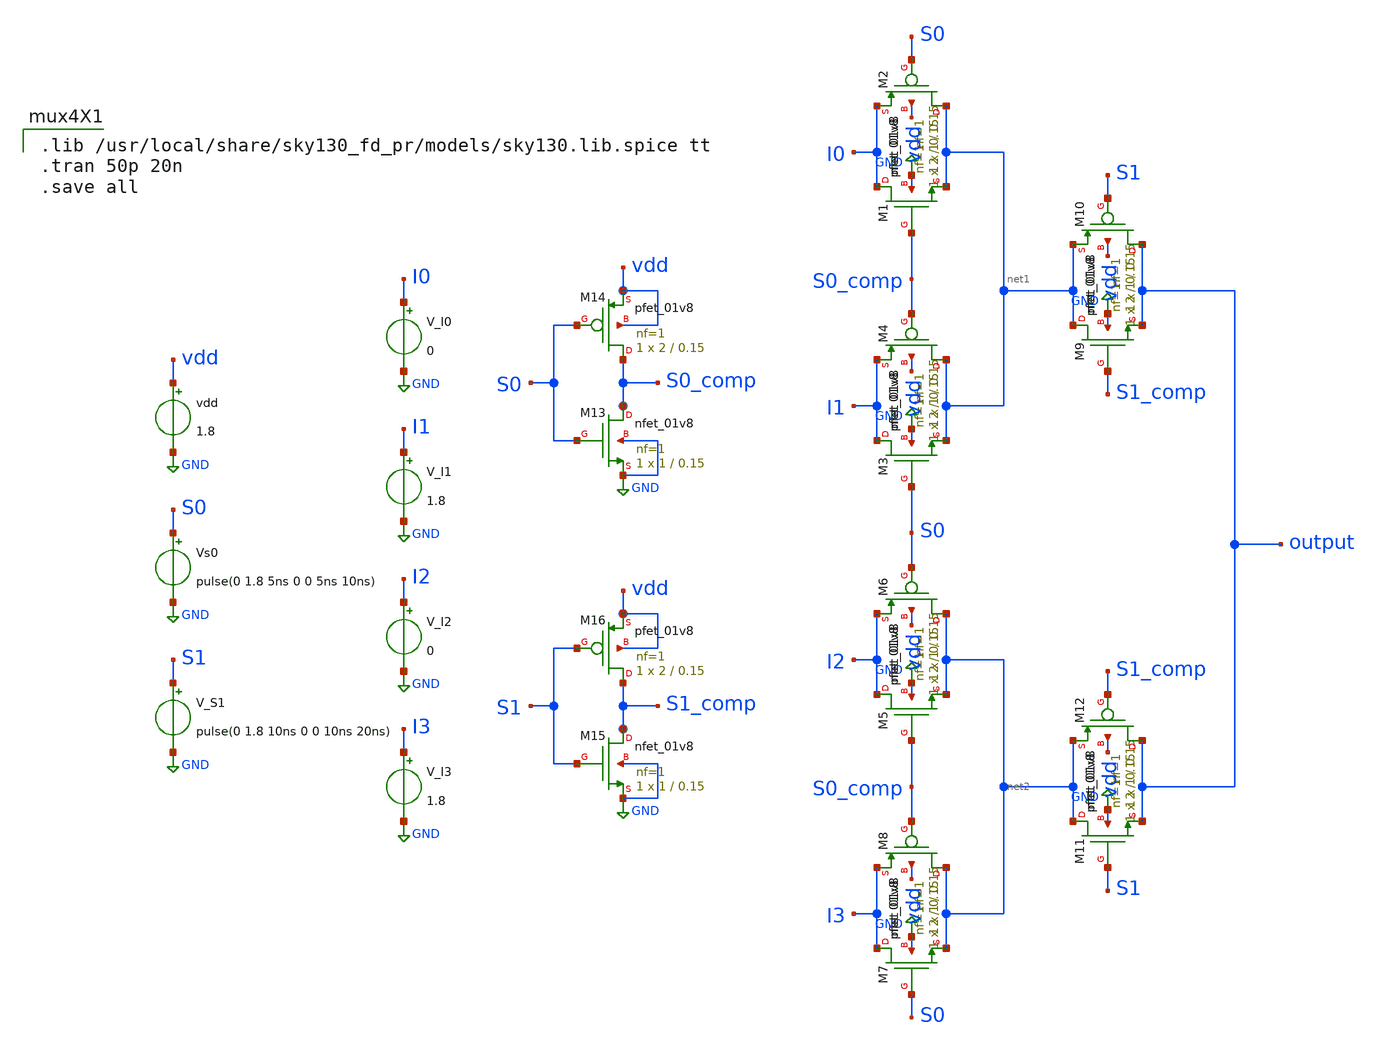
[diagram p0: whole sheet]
** sch_path: files/mux4X1.sch
**.subckt mux4X1
XM1 I0 S0_comp net1 GND sky130_fd_pr__nfet_01v8 L=0.15 W=1 nf=1 ad='int((1 + 1)/2) * 1 / 1 * 0.29' as='int((1 + 2)/2) * 1 / 1 * 0.29'
+ pd='2*int((1 + 1)/2) * (1 / 1 + 0.29)' ps='2*int((1 + 2)/2) * (1 / 1 + 0.29)' nrd='0.29 / 1 ' nrs='0.29 / 1 '
+ sa=0 sb=0 sd=0 mult=1 m=1
XM2 net1 S0 I0 vdd sky130_fd_pr__pfet_01v8 L=0.15 W=2 nf=1 ad='int((1 + 1)/2) * 2 / 1 * 0.29' as='int((1 + 2)/2) * 2 / 1 * 0.29'
+ pd='2*int((1 + 1)/2) * (2 / 1 + 0.29)' ps='2*int((1 + 2)/2) * (2 / 1 + 0.29)' nrd='0.29 / 2 ' nrs='0.29 / 2 '
+ sa=0 sb=0 sd=0 mult=1 m=1
XM3 I1 S0 net1 GND sky130_fd_pr__nfet_01v8 L=0.15 W=1 nf=1 ad='int((1 + 1)/2) * 1 / 1 * 0.29' as='int((1 + 2)/2) * 1 / 1 * 0.29'
+ pd='2*int((1 + 1)/2) * (1 / 1 + 0.29)' ps='2*int((1 + 2)/2) * (1 / 1 + 0.29)' nrd='0.29 / 1 ' nrs='0.29 / 1 '
+ sa=0 sb=0 sd=0 mult=1 m=1
XM4 net1 S0_comp I1 vdd sky130_fd_pr__pfet_01v8 L=0.15 W=2 nf=1 ad='int((1 + 1)/2) * 2 / 1 * 0.29' as='int((1 + 2)/2) * 2 / 1 * 0.29'
+ pd='2*int((1 + 1)/2) * (2 / 1 + 0.29)' ps='2*int((1 + 2)/2) * (2 / 1 + 0.29)' nrd='0.29 / 2 ' nrs='0.29 / 2 '
+ sa=0 sb=0 sd=0 mult=1 m=1
XM5 I2 S0_comp net2 GND sky130_fd_pr__nfet_01v8 L=0.15 W=1 nf=1 ad='int((1 + 1)/2) * 1 / 1 * 0.29' as='int((1 + 2)/2) * 1 / 1 * 0.29'
+ pd='2*int((1 + 1)/2) * (1 / 1 + 0.29)' ps='2*int((1 + 2)/2) * (1 / 1 + 0.29)' nrd='0.29 / 1 ' nrs='0.29 / 1 '
+ sa=0 sb=0 sd=0 mult=1 m=1
XM6 net2 S0 I2 vdd sky130_fd_pr__pfet_01v8 L=0.15 W=2 nf=1 ad='int((1 + 1)/2) * 2 / 1 * 0.29' as='int((1 + 2)/2) * 2 / 1 * 0.29'
+ pd='2*int((1 + 1)/2) * (2 / 1 + 0.29)' ps='2*int((1 + 2)/2) * (2 / 1 + 0.29)' nrd='0.29 / 2 ' nrs='0.29 / 2 '
+ sa=0 sb=0 sd=0 mult=1 m=1
XM7 I3 S0 net2 GND sky130_fd_pr__nfet_01v8 L=0.15 W=1 nf=1 ad='int((1 + 1)/2) * 1 / 1 * 0.29' as='int((1 + 2)/2) * 1 / 1 * 0.29'
+ pd='2*int((1 + 1)/2) * (1 / 1 + 0.29)' ps='2*int((1 + 2)/2) * (1 / 1 + 0.29)' nrd='0.29 / 1 ' nrs='0.29 / 1 '
+ sa=0 sb=0 sd=0 mult=1 m=1
XM8 net2 S0_comp I3 vdd sky130_fd_pr__pfet_01v8 L=0.15 W=2 nf=1 ad='int((1 + 1)/2) * 2 / 1 * 0.29' as='int((1 + 2)/2) * 2 / 1 * 0.29'
+ pd='2*int((1 + 1)/2) * (2 / 1 + 0.29)' ps='2*int((1 + 2)/2) * (2 / 1 + 0.29)' nrd='0.29 / 2 ' nrs='0.29 / 2 '
+ sa=0 sb=0 sd=0 mult=1 m=1
XM9 net1 S1_comp output GND sky130_fd_pr__nfet_01v8 L=0.15 W=1 nf=1 ad='int((1 + 1)/2) * 1 / 1 * 0.29'
+ as='int((1 + 2)/2) * 1 / 1 * 0.29' pd='2*int((1 + 1)/2) * (1 / 1 + 0.29)' ps='2*int((1 + 2)/2) * (1 / 1 + 0.29)'
+ nrd='0.29 / 1 ' nrs='0.29 / 1 ' sa=0 sb=0 sd=0 mult=1 m=1
XM10 output S1 net1 vdd sky130_fd_pr__pfet_01v8 L=0.15 W=2 nf=1 ad='int((1 + 1)/2) * 2 / 1 * 0.29' as='int((1 + 2)/2) * 2 / 1 * 0.29'
+ pd='2*int((1 + 1)/2) * (2 / 1 + 0.29)' ps='2*int((1 + 2)/2) * (2 / 1 + 0.29)' nrd='0.29 / 2 ' nrs='0.29 / 2 '
+ sa=0 sb=0 sd=0 mult=1 m=1
XM11 net2 S1 output GND sky130_fd_pr__nfet_01v8 L=0.15 W=1 nf=1 ad='int((1 + 1)/2) * 1 / 1 * 0.29' as='int((1 + 2)/2) * 1 / 1 * 0.29'
+ pd='2*int((1 + 1)/2) * (1 / 1 + 0.29)' ps='2*int((1 + 2)/2) * (1 / 1 + 0.29)' nrd='0.29 / 1 ' nrs='0.29 / 1 '
+ sa=0 sb=0 sd=0 mult=1 m=1
XM12 output S1_comp net2 vdd sky130_fd_pr__pfet_01v8 L=0.15 W=2 nf=1 ad='int((1 + 1)/2) * 2 / 1 * 0.29'
+ as='int((1 + 2)/2) * 2 / 1 * 0.29' pd='2*int((1 + 1)/2) * (2 / 1 + 0.29)' ps='2*int((1 + 2)/2) * (2 / 1 + 0.29)'
+ nrd='0.29 / 2 ' nrs='0.29 / 2 ' sa=0 sb=0 sd=0 mult=1 m=1
XM13 S0_comp S0 GND GND sky130_fd_pr__nfet_01v8 L=0.15 W=1 nf=1 ad='int((1 + 1)/2) * 1 / 1 * 0.29' as='int((1 + 2)/2) * 1 / 1 * 0.29'
+ pd='2*int((1 + 1)/2) * (1 / 1 + 0.29)' ps='2*int((1 + 2)/2) * (1 / 1 + 0.29)' nrd='0.29 / 1 ' nrs='0.29 / 1 '
+ sa=0 sb=0 sd=0 mult=1 m=1
XM14 S0_comp S0 vdd vdd sky130_fd_pr__pfet_01v8 L=0.15 W=2 nf=1 ad='int((1 + 1)/2) * 2 / 1 * 0.29' as='int((1 + 2)/2) * 2 / 1 * 0.29'
+ pd='2*int((1 + 1)/2) * (2 / 1 + 0.29)' ps='2*int((1 + 2)/2) * (2 / 1 + 0.29)' nrd='0.29 / 2 ' nrs='0.29 / 2 '
+ sa=0 sb=0 sd=0 mult=1 m=1
XM15 S1_comp S1 GND GND sky130_fd_pr__nfet_01v8 L=0.15 W=1 nf=1 ad='int((1 + 1)/2) * 1 / 1 * 0.29' as='int((1 + 2)/2) * 1 / 1 * 0.29'
+ pd='2*int((1 + 1)/2) * (1 / 1 + 0.29)' ps='2*int((1 + 2)/2) * (1 / 1 + 0.29)' nrd='0.29 / 1 ' nrs='0.29 / 1 '
+ sa=0 sb=0 sd=0 mult=1 m=1
XM16 S1_comp S1 vdd vdd sky130_fd_pr__pfet_01v8 L=0.15 W=2 nf=1 ad='int((1 + 1)/2) * 2 / 1 * 0.29' as='int((1 + 2)/2) * 2 / 1 * 0.29'
+ pd='2*int((1 + 1)/2) * (2 / 1 + 0.29)' ps='2*int((1 + 2)/2) * (2 / 1 + 0.29)' nrd='0.29 / 2 ' nrs='0.29 / 2 '
+ sa=0 sb=0 sd=0 mult=1 m=1
vdd vdd GND 1.8
Vs0 S0 GND pulse(0 1.8 5ns 0 0 5ns 10ns)
V_S1 S1 GND pulse(0 1.8 10ns 0 0 10ns 20ns)
V_I3 I3 GND 1.8
V_I0 I0 GND 0
V_I1 I1 GND 1.8
V_I2 I2 GND 0
**** begin user architecture code

.lib /usr/local/share/sky130_fd_pr/models/sky130.lib.spice tt
.tran 50p 20n
.save all

**** end user architecture code
**.ends
.GLOBAL GND
.end
